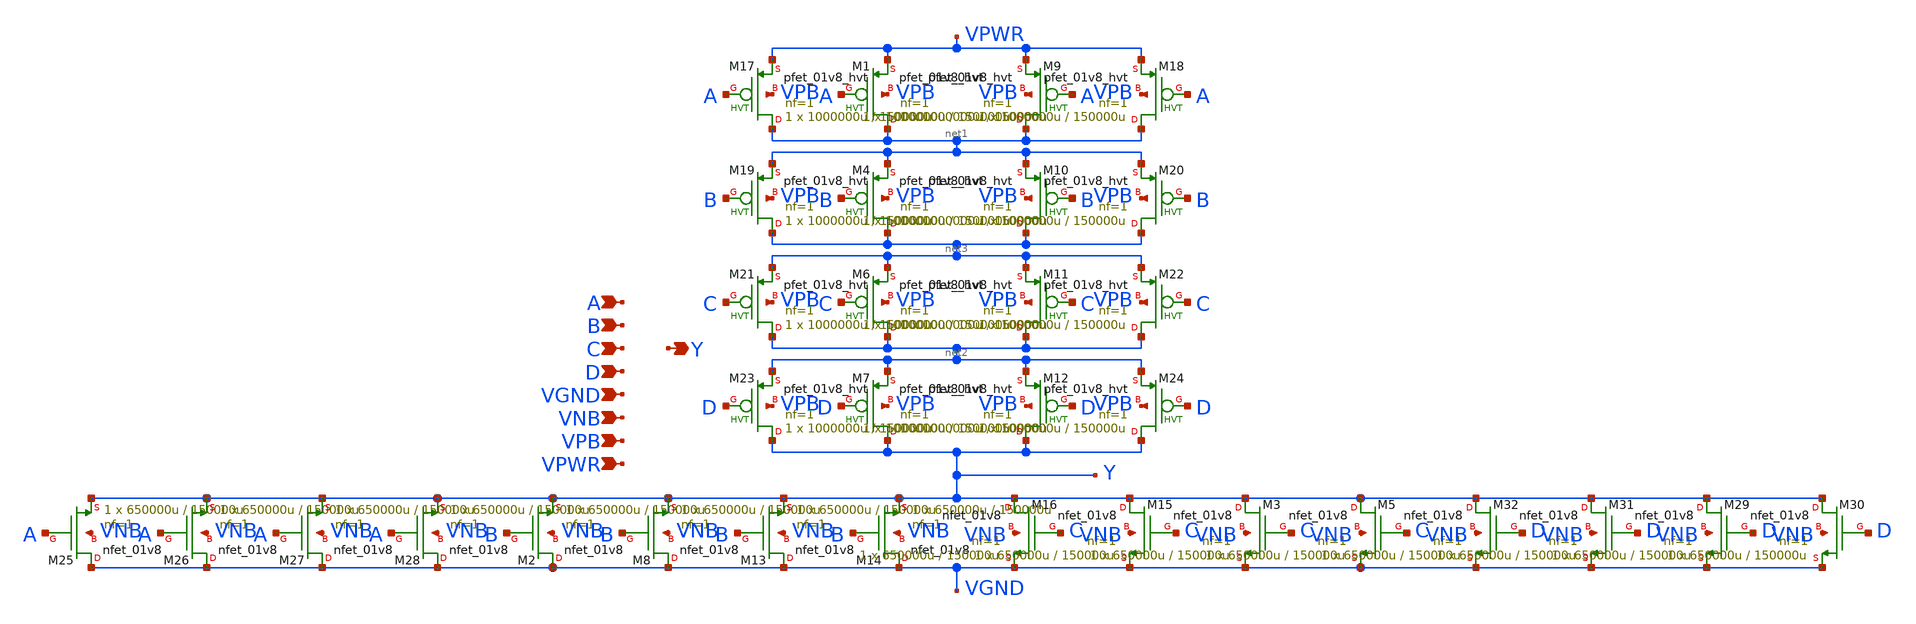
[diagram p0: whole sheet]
** sch_path: schematics/nor4/sky130_fd_sc_hd__nor4_4.sch
**.subckt sky130_fd_sc_hd__nor4_4 A B C D VGND VNB VPB VPWR Y
*.ipin A
*.ipin B
*.ipin C
*.ipin D
*.ipin VGND
*.ipin VNB
*.ipin VPB
*.ipin VPWR
*.opin Y
XM1 net1 A VPWR VPB sky130_fd_pr__pfet_01v8_hvt L=150000u W=1000000u nf=1 ad='int((1 + 1)/2) * 1000000u / 1 * 0.29'
+ as='int((1 + 2)/2) * 1000000u / 1 * 0.29' pd='2*int((1 + 1)/2) * (1000000u / 1 + 0.29)' ps='2*int((1 + 2)/2) * (1000000u / 1 + 0.29)'
+ nrd='0.29 / 1000000u ' nrs='0.29 / 1000000u ' sa=0 sb=0 sd=0 mult=1 m=1
XM2 VGND B Y VNB sky130_fd_pr__nfet_01v8 L=150000u W=650000u nf=1 ad='int((1 + 1)/2) * 650000u / 1 * 0.29'
+ as='int((1 + 2)/2) * 650000u / 1 * 0.29' pd='2*int((1 + 1)/2) * (650000u / 1 + 0.29)' ps='2*int((1 + 2)/2) * (650000u / 1 + 0.29)'
+ nrd='0.29 / 650000u ' nrs='0.29 / 650000u ' sa=0 sb=0 sd=0 mult=1 m=1
XM4 net3 B net1 VPB sky130_fd_pr__pfet_01v8_hvt L=150000u W=1000000u nf=1 ad='int((1 + 1)/2) * 1000000u / 1 * 0.29'
+ as='int((1 + 2)/2) * 1000000u / 1 * 0.29' pd='2*int((1 + 1)/2) * (1000000u / 1 + 0.29)' ps='2*int((1 + 2)/2) * (1000000u / 1 + 0.29)'
+ nrd='0.29 / 1000000u ' nrs='0.29 / 1000000u ' sa=0 sb=0 sd=0 mult=1 m=1
XM3 Y C VGND VNB sky130_fd_pr__nfet_01v8 L=150000u W=650000u nf=1 ad='int((1 + 1)/2) * 650000u / 1 * 0.29'
+ as='int((1 + 2)/2) * 650000u / 1 * 0.29' pd='2*int((1 + 1)/2) * (650000u / 1 + 0.29)' ps='2*int((1 + 2)/2) * (650000u / 1 + 0.29)'
+ nrd='0.29 / 650000u ' nrs='0.29 / 650000u ' sa=0 sb=0 sd=0 mult=1 m=1
XM5 Y C VGND VNB sky130_fd_pr__nfet_01v8 L=150000u W=650000u nf=1 ad='int((1 + 1)/2) * 650000u / 1 * 0.29'
+ as='int((1 + 2)/2) * 650000u / 1 * 0.29' pd='2*int((1 + 1)/2) * (650000u / 1 + 0.29)' ps='2*int((1 + 2)/2) * (650000u / 1 + 0.29)'
+ nrd='0.29 / 650000u ' nrs='0.29 / 650000u ' sa=0 sb=0 sd=0 mult=1 m=1
XM6 net2 C net3 VPB sky130_fd_pr__pfet_01v8_hvt L=150000u W=1000000u nf=1 ad='int((1 + 1)/2) * 1000000u / 1 * 0.29'
+ as='int((1 + 2)/2) * 1000000u / 1 * 0.29' pd='2*int((1 + 1)/2) * (1000000u / 1 + 0.29)' ps='2*int((1 + 2)/2) * (1000000u / 1 + 0.29)'
+ nrd='0.29 / 1000000u ' nrs='0.29 / 1000000u ' sa=0 sb=0 sd=0 mult=1 m=1
XM7 Y D net2 VPB sky130_fd_pr__pfet_01v8_hvt L=150000u W=1000000u nf=1 ad='int((1 + 1)/2) * 1000000u / 1 * 0.29'
+ as='int((1 + 2)/2) * 1000000u / 1 * 0.29' pd='2*int((1 + 1)/2) * (1000000u / 1 + 0.29)' ps='2*int((1 + 2)/2) * (1000000u / 1 + 0.29)'
+ nrd='0.29 / 1000000u ' nrs='0.29 / 1000000u ' sa=0 sb=0 sd=0 mult=1 m=1
XM8 VGND B Y VNB sky130_fd_pr__nfet_01v8 L=150000u W=650000u nf=1 ad='int((1 + 1)/2) * 650000u / 1 * 0.29'
+ as='int((1 + 2)/2) * 650000u / 1 * 0.29' pd='2*int((1 + 1)/2) * (650000u / 1 + 0.29)' ps='2*int((1 + 2)/2) * (650000u / 1 + 0.29)'
+ nrd='0.29 / 650000u ' nrs='0.29 / 650000u ' sa=0 sb=0 sd=0 mult=1 m=1
XM9 net1 A VPWR VPB sky130_fd_pr__pfet_01v8_hvt L=150000u W=1000000u nf=1 ad='int((1 + 1)/2) * 1000000u / 1 * 0.29'
+ as='int((1 + 2)/2) * 1000000u / 1 * 0.29' pd='2*int((1 + 1)/2) * (1000000u / 1 + 0.29)' ps='2*int((1 + 2)/2) * (1000000u / 1 + 0.29)'
+ nrd='0.29 / 1000000u ' nrs='0.29 / 1000000u ' sa=0 sb=0 sd=0 mult=1 m=1
XM10 net3 B net1 VPB sky130_fd_pr__pfet_01v8_hvt L=150000u W=1000000u nf=1 ad='int((1 + 1)/2) * 1000000u / 1 * 0.29'
+ as='int((1 + 2)/2) * 1000000u / 1 * 0.29' pd='2*int((1 + 1)/2) * (1000000u / 1 + 0.29)' ps='2*int((1 + 2)/2) * (1000000u / 1 + 0.29)'
+ nrd='0.29 / 1000000u ' nrs='0.29 / 1000000u ' sa=0 sb=0 sd=0 mult=1 m=1
XM11 net2 C net3 VPB sky130_fd_pr__pfet_01v8_hvt L=150000u W=1000000u nf=1 ad='int((1 + 1)/2) * 1000000u / 1 * 0.29'
+ as='int((1 + 2)/2) * 1000000u / 1 * 0.29' pd='2*int((1 + 1)/2) * (1000000u / 1 + 0.29)' ps='2*int((1 + 2)/2) * (1000000u / 1 + 0.29)'
+ nrd='0.29 / 1000000u ' nrs='0.29 / 1000000u ' sa=0 sb=0 sd=0 mult=1 m=1
XM12 Y D net2 VPB sky130_fd_pr__pfet_01v8_hvt L=150000u W=1000000u nf=1 ad='int((1 + 1)/2) * 1000000u / 1 * 0.29'
+ as='int((1 + 2)/2) * 1000000u / 1 * 0.29' pd='2*int((1 + 1)/2) * (1000000u / 1 + 0.29)' ps='2*int((1 + 2)/2) * (1000000u / 1 + 0.29)'
+ nrd='0.29 / 1000000u ' nrs='0.29 / 1000000u ' sa=0 sb=0 sd=0 mult=1 m=1
XM13 VGND B Y VNB sky130_fd_pr__nfet_01v8 L=150000u W=650000u nf=1 ad='int((1 + 1)/2) * 650000u / 1 * 0.29'
+ as='int((1 + 2)/2) * 650000u / 1 * 0.29' pd='2*int((1 + 1)/2) * (650000u / 1 + 0.29)' ps='2*int((1 + 2)/2) * (650000u / 1 + 0.29)'
+ nrd='0.29 / 650000u ' nrs='0.29 / 650000u ' sa=0 sb=0 sd=0 mult=1 m=1
XM14 VGND B Y VNB sky130_fd_pr__nfet_01v8 L=150000u W=650000u nf=1 ad='int((1 + 1)/2) * 650000u / 1 * 0.29'
+ as='int((1 + 2)/2) * 650000u / 1 * 0.29' pd='2*int((1 + 1)/2) * (650000u / 1 + 0.29)' ps='2*int((1 + 2)/2) * (650000u / 1 + 0.29)'
+ nrd='0.29 / 650000u ' nrs='0.29 / 650000u ' sa=0 sb=0 sd=0 mult=1 m=1
XM15 Y C VGND VNB sky130_fd_pr__nfet_01v8 L=150000u W=650000u nf=1 ad='int((1 + 1)/2) * 650000u / 1 * 0.29'
+ as='int((1 + 2)/2) * 650000u / 1 * 0.29' pd='2*int((1 + 1)/2) * (650000u / 1 + 0.29)' ps='2*int((1 + 2)/2) * (650000u / 1 + 0.29)'
+ nrd='0.29 / 650000u ' nrs='0.29 / 650000u ' sa=0 sb=0 sd=0 mult=1 m=1
XM16 Y C VGND VNB sky130_fd_pr__nfet_01v8 L=150000u W=650000u nf=1 ad='int((1 + 1)/2) * 650000u / 1 * 0.29'
+ as='int((1 + 2)/2) * 650000u / 1 * 0.29' pd='2*int((1 + 1)/2) * (650000u / 1 + 0.29)' ps='2*int((1 + 2)/2) * (650000u / 1 + 0.29)'
+ nrd='0.29 / 650000u ' nrs='0.29 / 650000u ' sa=0 sb=0 sd=0 mult=1 m=1
XM17 net1 A VPWR VPB sky130_fd_pr__pfet_01v8_hvt L=150000u W=1000000u nf=1 ad='int((1 + 1)/2) * 1000000u / 1 * 0.29'
+ as='int((1 + 2)/2) * 1000000u / 1 * 0.29' pd='2*int((1 + 1)/2) * (1000000u / 1 + 0.29)' ps='2*int((1 + 2)/2) * (1000000u / 1 + 0.29)'
+ nrd='0.29 / 1000000u ' nrs='0.29 / 1000000u ' sa=0 sb=0 sd=0 mult=1 m=1
XM18 net1 A VPWR VPB sky130_fd_pr__pfet_01v8_hvt L=150000u W=1000000u nf=1 ad='int((1 + 1)/2) * 1000000u / 1 * 0.29'
+ as='int((1 + 2)/2) * 1000000u / 1 * 0.29' pd='2*int((1 + 1)/2) * (1000000u / 1 + 0.29)' ps='2*int((1 + 2)/2) * (1000000u / 1 + 0.29)'
+ nrd='0.29 / 1000000u ' nrs='0.29 / 1000000u ' sa=0 sb=0 sd=0 mult=1 m=1
XM19 net3 B net1 VPB sky130_fd_pr__pfet_01v8_hvt L=150000u W=1000000u nf=1 ad='int((1 + 1)/2) * 1000000u / 1 * 0.29'
+ as='int((1 + 2)/2) * 1000000u / 1 * 0.29' pd='2*int((1 + 1)/2) * (1000000u / 1 + 0.29)' ps='2*int((1 + 2)/2) * (1000000u / 1 + 0.29)'
+ nrd='0.29 / 1000000u ' nrs='0.29 / 1000000u ' sa=0 sb=0 sd=0 mult=1 m=1
XM20 net3 B net1 VPB sky130_fd_pr__pfet_01v8_hvt L=150000u W=1000000u nf=1 ad='int((1 + 1)/2) * 1000000u / 1 * 0.29'
+ as='int((1 + 2)/2) * 1000000u / 1 * 0.29' pd='2*int((1 + 1)/2) * (1000000u / 1 + 0.29)' ps='2*int((1 + 2)/2) * (1000000u / 1 + 0.29)'
+ nrd='0.29 / 1000000u ' nrs='0.29 / 1000000u ' sa=0 sb=0 sd=0 mult=1 m=1
XM21 net2 C net3 VPB sky130_fd_pr__pfet_01v8_hvt L=150000u W=1000000u nf=1 ad='int((1 + 1)/2) * 1000000u / 1 * 0.29'
+ as='int((1 + 2)/2) * 1000000u / 1 * 0.29' pd='2*int((1 + 1)/2) * (1000000u / 1 + 0.29)' ps='2*int((1 + 2)/2) * (1000000u / 1 + 0.29)'
+ nrd='0.29 / 1000000u ' nrs='0.29 / 1000000u ' sa=0 sb=0 sd=0 mult=1 m=1
XM22 net2 C net3 VPB sky130_fd_pr__pfet_01v8_hvt L=150000u W=1000000u nf=1 ad='int((1 + 1)/2) * 1000000u / 1 * 0.29'
+ as='int((1 + 2)/2) * 1000000u / 1 * 0.29' pd='2*int((1 + 1)/2) * (1000000u / 1 + 0.29)' ps='2*int((1 + 2)/2) * (1000000u / 1 + 0.29)'
+ nrd='0.29 / 1000000u ' nrs='0.29 / 1000000u ' sa=0 sb=0 sd=0 mult=1 m=1
XM23 Y D net2 VPB sky130_fd_pr__pfet_01v8_hvt L=150000u W=1000000u nf=1 ad='int((1 + 1)/2) * 1000000u / 1 * 0.29'
+ as='int((1 + 2)/2) * 1000000u / 1 * 0.29' pd='2*int((1 + 1)/2) * (1000000u / 1 + 0.29)' ps='2*int((1 + 2)/2) * (1000000u / 1 + 0.29)'
+ nrd='0.29 / 1000000u ' nrs='0.29 / 1000000u ' sa=0 sb=0 sd=0 mult=1 m=1
XM24 Y D net2 VPB sky130_fd_pr__pfet_01v8_hvt L=150000u W=1000000u nf=1 ad='int((1 + 1)/2) * 1000000u / 1 * 0.29'
+ as='int((1 + 2)/2) * 1000000u / 1 * 0.29' pd='2*int((1 + 1)/2) * (1000000u / 1 + 0.29)' ps='2*int((1 + 2)/2) * (1000000u / 1 + 0.29)'
+ nrd='0.29 / 1000000u ' nrs='0.29 / 1000000u ' sa=0 sb=0 sd=0 mult=1 m=1
XM25 VGND A Y VNB sky130_fd_pr__nfet_01v8 L=150000u W=650000u nf=1 ad='int((1 + 1)/2) * 650000u / 1 * 0.29'
+ as='int((1 + 2)/2) * 650000u / 1 * 0.29' pd='2*int((1 + 1)/2) * (650000u / 1 + 0.29)' ps='2*int((1 + 2)/2) * (650000u / 1 + 0.29)'
+ nrd='0.29 / 650000u ' nrs='0.29 / 650000u ' sa=0 sb=0 sd=0 mult=1 m=1
XM26 VGND A Y VNB sky130_fd_pr__nfet_01v8 L=150000u W=650000u nf=1 ad='int((1 + 1)/2) * 650000u / 1 * 0.29'
+ as='int((1 + 2)/2) * 650000u / 1 * 0.29' pd='2*int((1 + 1)/2) * (650000u / 1 + 0.29)' ps='2*int((1 + 2)/2) * (650000u / 1 + 0.29)'
+ nrd='0.29 / 650000u ' nrs='0.29 / 650000u ' sa=0 sb=0 sd=0 mult=1 m=1
XM27 VGND A Y VNB sky130_fd_pr__nfet_01v8 L=150000u W=650000u nf=1 ad='int((1 + 1)/2) * 650000u / 1 * 0.29'
+ as='int((1 + 2)/2) * 650000u / 1 * 0.29' pd='2*int((1 + 1)/2) * (650000u / 1 + 0.29)' ps='2*int((1 + 2)/2) * (650000u / 1 + 0.29)'
+ nrd='0.29 / 650000u ' nrs='0.29 / 650000u ' sa=0 sb=0 sd=0 mult=1 m=1
XM28 VGND A Y VNB sky130_fd_pr__nfet_01v8 L=150000u W=650000u nf=1 ad='int((1 + 1)/2) * 650000u / 1 * 0.29'
+ as='int((1 + 2)/2) * 650000u / 1 * 0.29' pd='2*int((1 + 1)/2) * (650000u / 1 + 0.29)' ps='2*int((1 + 2)/2) * (650000u / 1 + 0.29)'
+ nrd='0.29 / 650000u ' nrs='0.29 / 650000u ' sa=0 sb=0 sd=0 mult=1 m=1
XM29 Y D VGND VNB sky130_fd_pr__nfet_01v8 L=150000u W=650000u nf=1 ad='int((1 + 1)/2) * 650000u / 1 * 0.29'
+ as='int((1 + 2)/2) * 650000u / 1 * 0.29' pd='2*int((1 + 1)/2) * (650000u / 1 + 0.29)' ps='2*int((1 + 2)/2) * (650000u / 1 + 0.29)'
+ nrd='0.29 / 650000u ' nrs='0.29 / 650000u ' sa=0 sb=0 sd=0 mult=1 m=1
XM30 Y D VGND VNB sky130_fd_pr__nfet_01v8 L=150000u W=650000u nf=1 ad='int((1 + 1)/2) * 650000u / 1 * 0.29'
+ as='int((1 + 2)/2) * 650000u / 1 * 0.29' pd='2*int((1 + 1)/2) * (650000u / 1 + 0.29)' ps='2*int((1 + 2)/2) * (650000u / 1 + 0.29)'
+ nrd='0.29 / 650000u ' nrs='0.29 / 650000u ' sa=0 sb=0 sd=0 mult=1 m=1
XM31 Y D VGND VNB sky130_fd_pr__nfet_01v8 L=150000u W=650000u nf=1 ad='int((1 + 1)/2) * 650000u / 1 * 0.29'
+ as='int((1 + 2)/2) * 650000u / 1 * 0.29' pd='2*int((1 + 1)/2) * (650000u / 1 + 0.29)' ps='2*int((1 + 2)/2) * (650000u / 1 + 0.29)'
+ nrd='0.29 / 650000u ' nrs='0.29 / 650000u ' sa=0 sb=0 sd=0 mult=1 m=1
XM32 Y D VGND VNB sky130_fd_pr__nfet_01v8 L=150000u W=650000u nf=1 ad='int((1 + 1)/2) * 650000u / 1 * 0.29'
+ as='int((1 + 2)/2) * 650000u / 1 * 0.29' pd='2*int((1 + 1)/2) * (650000u / 1 + 0.29)' ps='2*int((1 + 2)/2) * (650000u / 1 + 0.29)'
+ nrd='0.29 / 650000u ' nrs='0.29 / 650000u ' sa=0 sb=0 sd=0 mult=1 m=1
**.ends
.end
